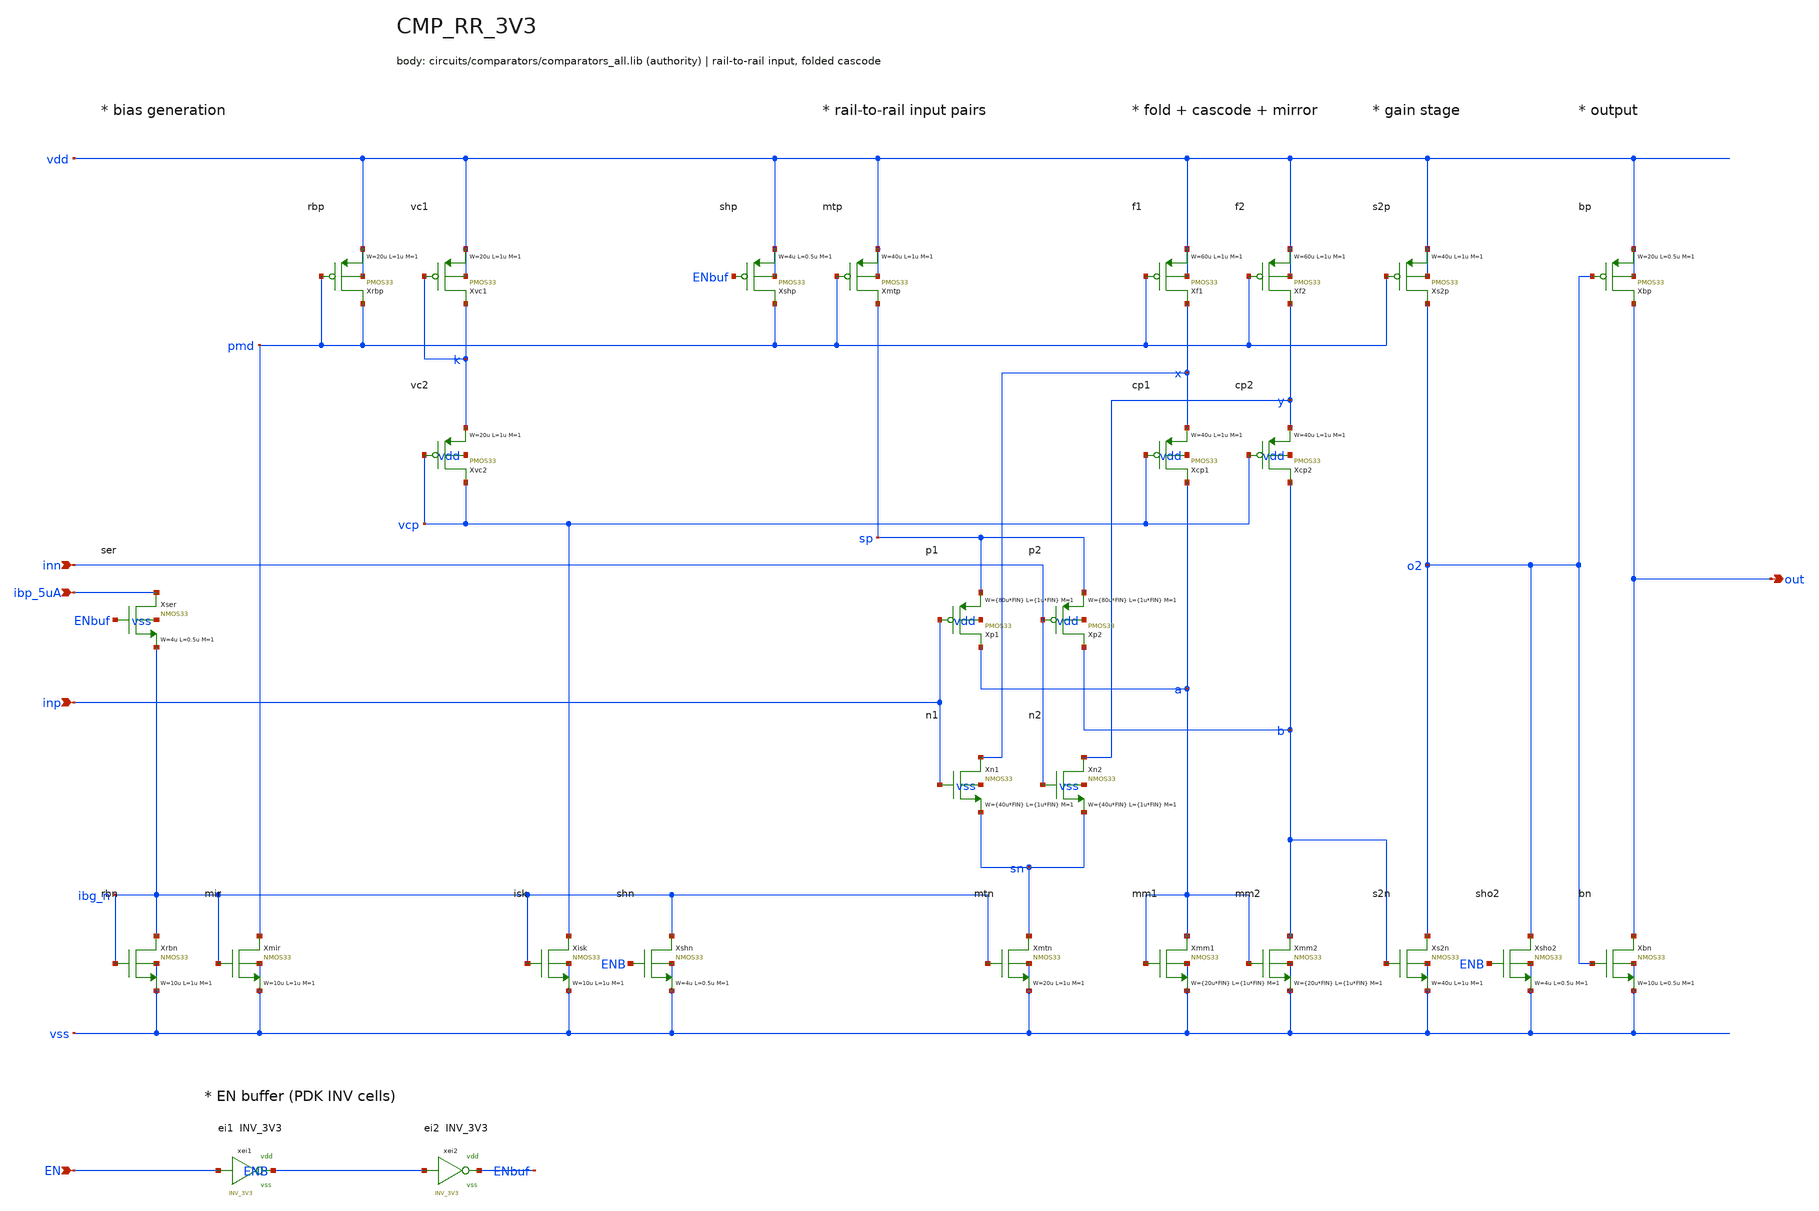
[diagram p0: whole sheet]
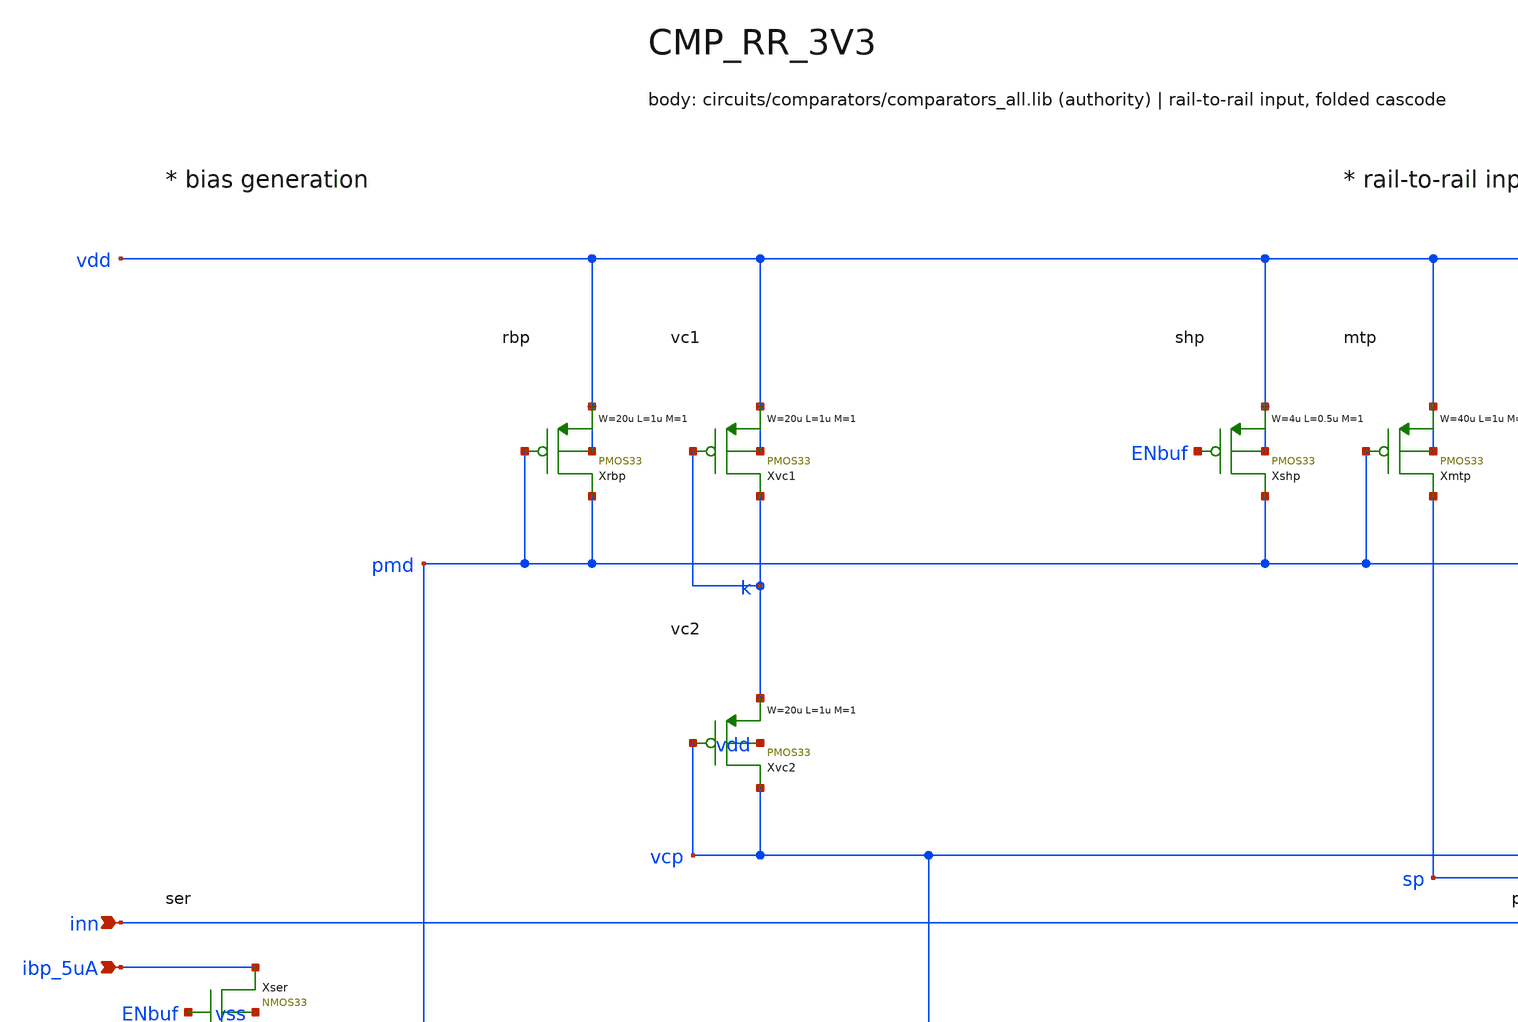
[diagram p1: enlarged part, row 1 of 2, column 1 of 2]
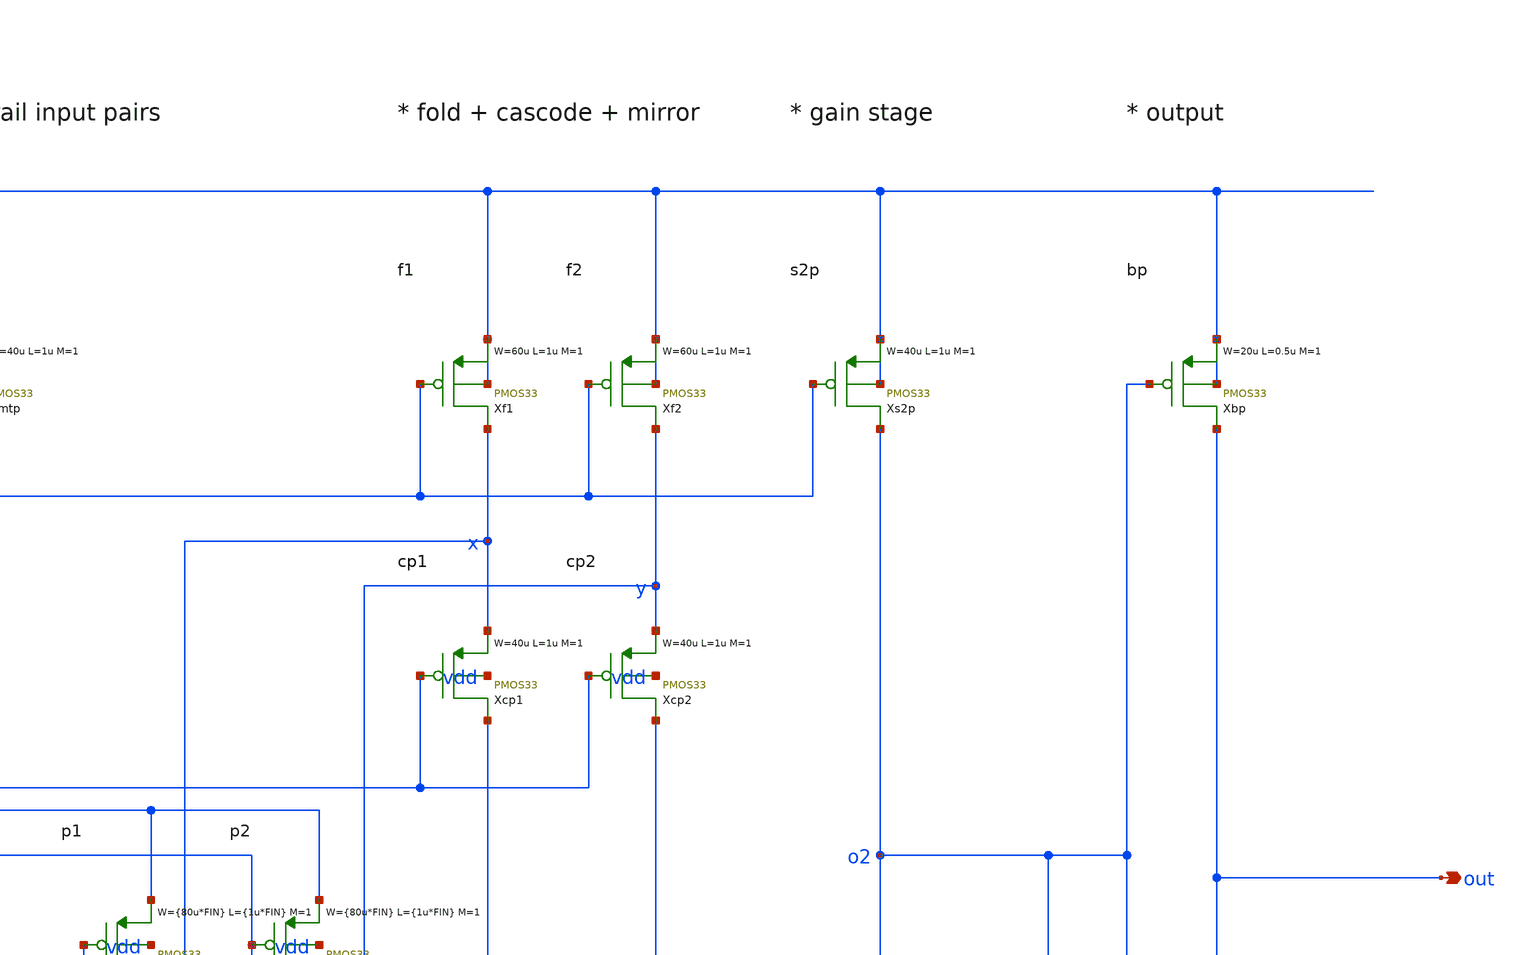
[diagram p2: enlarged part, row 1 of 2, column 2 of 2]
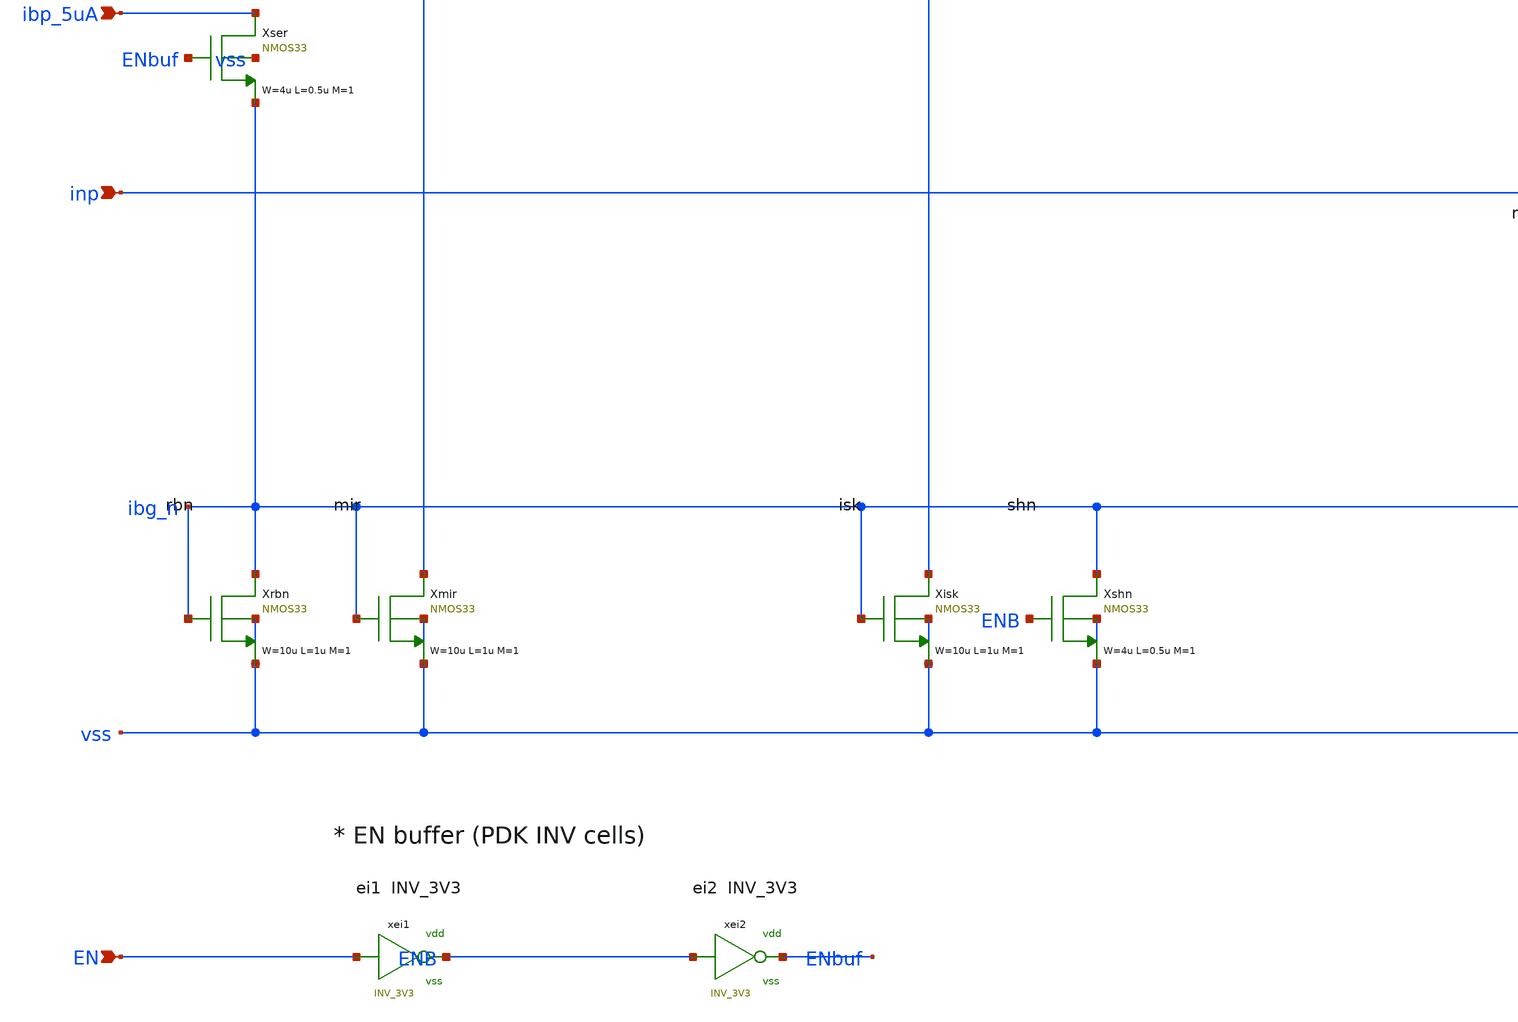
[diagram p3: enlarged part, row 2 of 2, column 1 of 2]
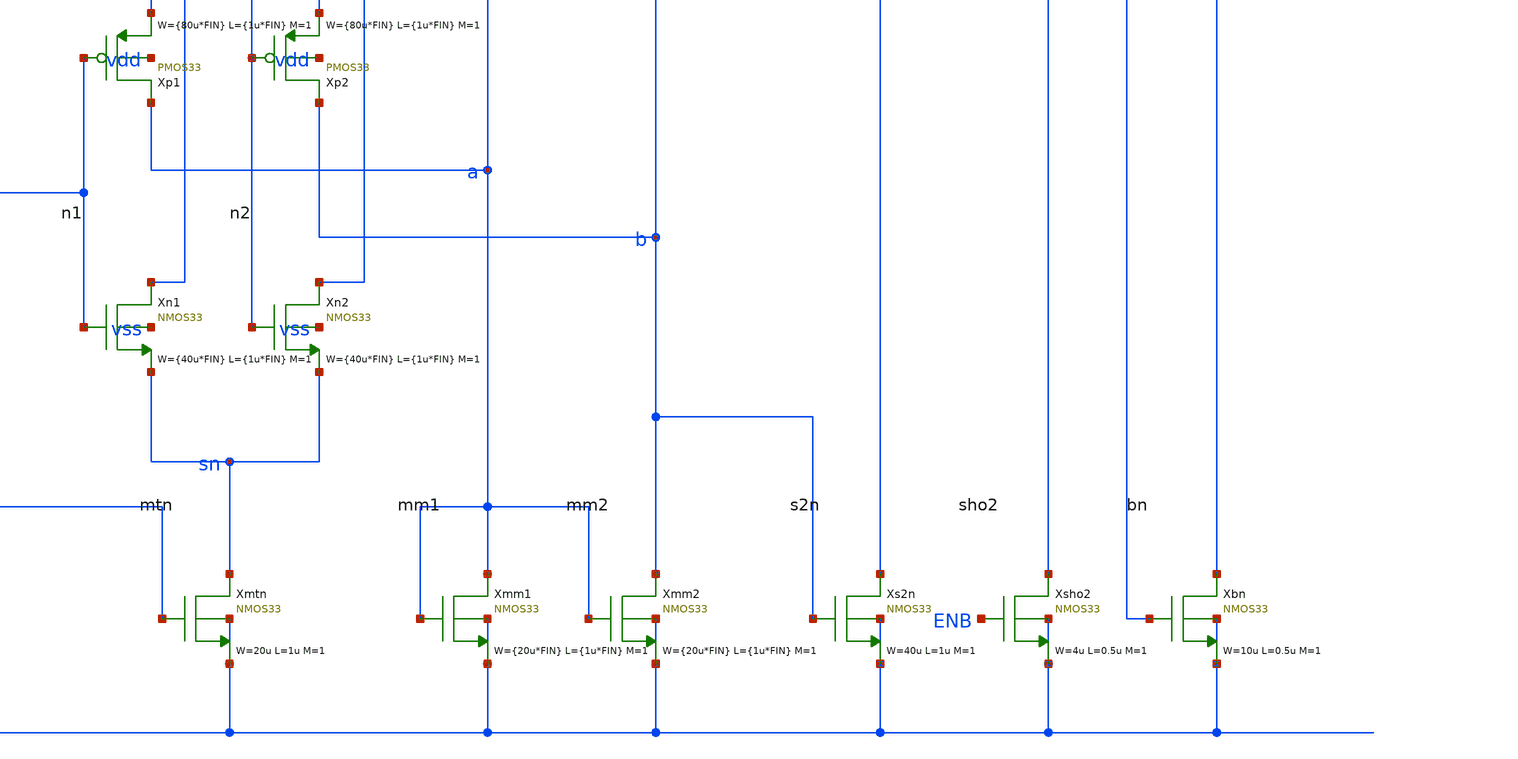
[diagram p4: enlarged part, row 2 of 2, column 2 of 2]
** sch_path: xschem/comparators/CMP_RR_3V3.sch
**.subckt CMP_RR_3V3 ibp_5uA out inp inn EN
*.ipin ibp_5uA
*.opin out
*.ipin inp
*.ipin inn
*.ipin EN
Xrbn ibg_n ibg_n vss vss NMOS33 W=10u L=1u M=1 MM_SIGMA=0
Xser ibp_5uA ENbuf ibg_n vss NMOS33 W=4u L=0.5u M=1 MM_SIGMA=0
Xmir pmd ibg_n vss vss NMOS33 W=10u L=1u M=1 MM_SIGMA=0
Xrbp pmd pmd vdd vdd PMOS33 W=20u L=1u M=1 MM_SIGMA=0
Xvc1 k k vdd vdd PMOS33 W=20u L=1u M=1 MM_SIGMA=0
Xvc2 vcp vcp k vdd PMOS33 W=20u L=1u M=1 MM_SIGMA=0
Xisk vcp ibg_n vss vss NMOS33 W=10u L=1u M=1 MM_SIGMA=0
Xshn ibg_n ENB vss vss NMOS33 W=4u L=0.5u M=1 MM_SIGMA=0
Xshp pmd ENbuf vdd vdd PMOS33 W=4u L=0.5u M=1 MM_SIGMA=0
Xmtp sp pmd vdd vdd PMOS33 W=40u L=1u M=1 MM_SIGMA=0
Xp1 a inp sp vdd PMOS33 W={80u*FIN} L={1u*FIN} M=1 MM_SIGMA=0
Xp2 b inn sp vdd PMOS33 W={80u*FIN} L={1u*FIN} M=1 MM_SIGMA=0
Xn1 x inp sn vss NMOS33 W={40u*FIN} L={1u*FIN} M=1 MM_SIGMA=0
Xn2 y inn sn vss NMOS33 W={40u*FIN} L={1u*FIN} M=1 MM_SIGMA=0
Xmtn sn ibg_n vss vss NMOS33 W=20u L=1u M=1 MM_SIGMA=0
Xf1 x pmd vdd vdd PMOS33 W=60u L=1u M=1 MM_SIGMA=0
Xcp1 a vcp x vdd PMOS33 W=40u L=1u M=1 MM_SIGMA=0
Xmm1 a a vss vss NMOS33 W={20u*FIN} L={1u*FIN} M=1 MM_SIGMA=0
Xf2 y pmd vdd vdd PMOS33 W=60u L=1u M=1 MM_SIGMA=0
Xcp2 b vcp y vdd PMOS33 W=40u L=1u M=1 MM_SIGMA=0
Xmm2 b a vss vss NMOS33 W={20u*FIN} L={1u*FIN} M=1 MM_SIGMA=0
Xs2p o2 pmd vdd vdd PMOS33 W=40u L=1u M=1 MM_SIGMA=0
Xs2n o2 b vss vss NMOS33 W=40u L=1u M=1 MM_SIGMA=0
Xsho2 o2 ENB vss vss NMOS33 W=4u L=0.5u M=1 MM_SIGMA=0
Xbp out o2 vdd vdd PMOS33 W=20u L=0.5u M=1 MM_SIGMA=0
Xbn out o2 vss vss NMOS33 W=10u L=0.5u M=1 MM_SIGMA=0
xei1 EN ENB vdd vss INV_3V3
xei2 ENB ENbuf vdd vss INV_3V3
**.ends

* expanding   symbol:  logic/INV_3V3.sym # of pins=2
** sym_path: xschem/logic/INV_3V3.sym
* INV_3V3 body is defined in circuits/async_logic_design/cells.lib
.end
